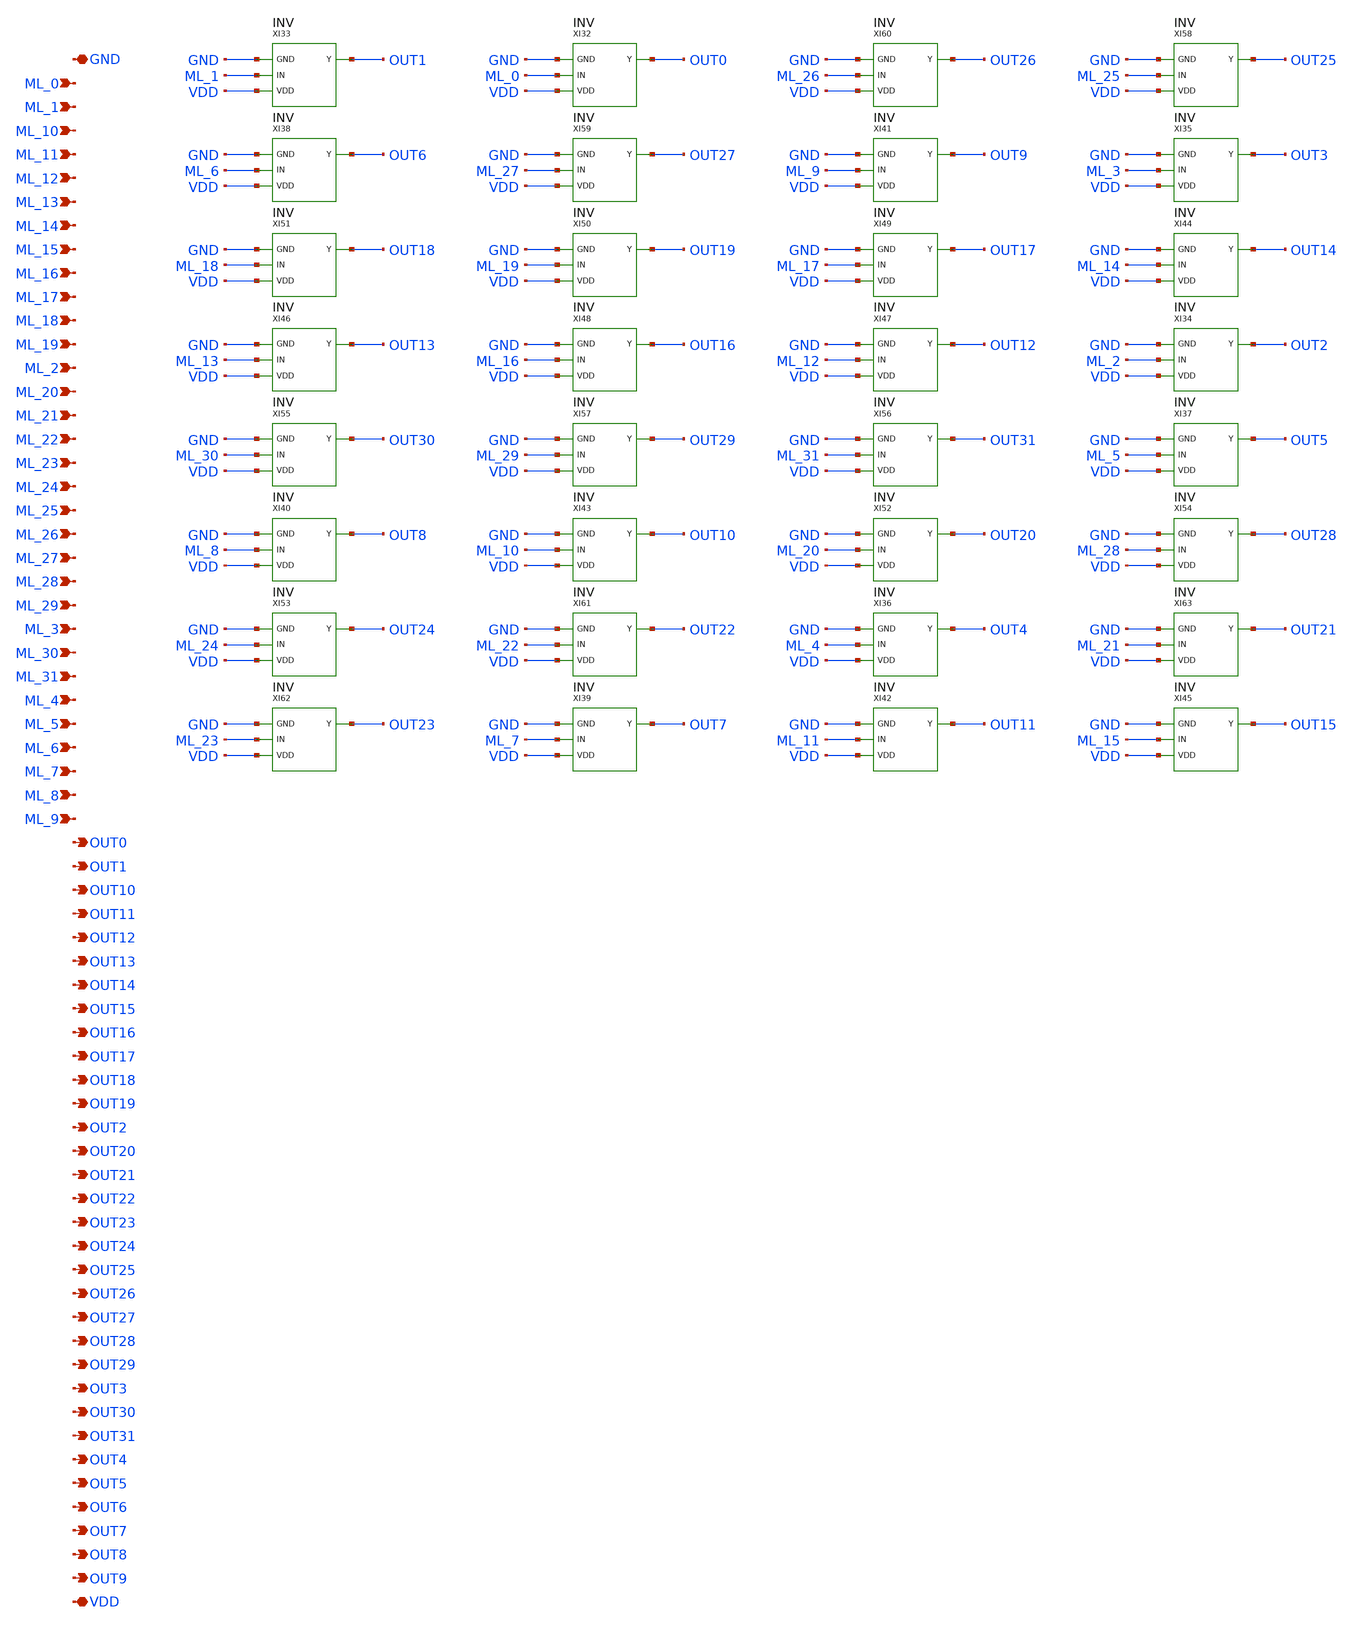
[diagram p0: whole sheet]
** sch_path: SoC6169-main/schematic/xschem/inverter_sens.sch
* Copyright 2026 USFQ CAM team
* Licensed under the Apache License, Version 2.0 (the "License");
* you may not use this file except in compliance with the License.
* You may obtain a copy of the License at
* https://www.apache.org/licenses/LICENSE-2.0
* Unless required by applicable law or agreed to in writing, software
* distributed under the License is distributed on an "AS IS" BASIS,
* WITHOUT WARRANTIES OR CONDITIONS OF ANY KIND, either express or implied.
* See the License for the specific language governing permissions and
* limitations under the License.
**.subckt inverter_sens GND ML_0 ML_1 ML_10 ML_11 ML_12 ML_13 ML_14 ML_15 ML_16 ML_17 ML_18 ML_19
*+ ML_2 ML_20 ML_21 ML_22 ML_23 ML_24 ML_25 ML_26 ML_27 ML_28 ML_29 ML_3 ML_30 ML_31 ML_4 ML_5 ML_6 ML_7
*+ ML_8 ML_9 OUT0 OUT1 OUT10 OUT11 OUT12 OUT13 OUT14 OUT15 OUT16 OUT17 OUT18 OUT19 OUT2 OUT20 OUT21 OUT22
*+ OUT23 OUT24 OUT25 OUT26 OUT27 OUT28 OUT29 OUT3 OUT30 OUT31 OUT4 OUT5 OUT6 OUT7 OUT8 OUT9 VDD
*.iopin GND
*.ipin ML_0
*.ipin ML_1
*.ipin ML_10
*.ipin ML_11
*.ipin ML_12
*.ipin ML_13
*.ipin ML_14
*.ipin ML_15
*.ipin ML_16
*.ipin ML_17
*.ipin ML_18
*.ipin ML_19
*.ipin ML_2
*.ipin ML_20
*.ipin ML_21
*.ipin ML_22
*.ipin ML_23
*.ipin ML_24
*.ipin ML_25
*.ipin ML_26
*.ipin ML_27
*.ipin ML_28
*.ipin ML_29
*.ipin ML_3
*.ipin ML_30
*.ipin ML_31
*.ipin ML_4
*.ipin ML_5
*.ipin ML_6
*.ipin ML_7
*.ipin ML_8
*.ipin ML_9
*.opin OUT0
*.opin OUT1
*.opin OUT10
*.opin OUT11
*.opin OUT12
*.opin OUT13
*.opin OUT14
*.opin OUT15
*.opin OUT16
*.opin OUT17
*.opin OUT18
*.opin OUT19
*.opin OUT2
*.opin OUT20
*.opin OUT21
*.opin OUT22
*.opin OUT23
*.opin OUT24
*.opin OUT25
*.opin OUT26
*.opin OUT27
*.opin OUT28
*.opin OUT29
*.opin OUT3
*.opin OUT30
*.opin OUT31
*.opin OUT4
*.opin OUT5
*.opin OUT6
*.opin OUT7
*.opin OUT8
*.opin OUT9
*.iopin VDD
XI33 GND ML_1 VDD OUT1 INV
XI32 GND ML_0 VDD OUT0 INV
XI60 GND ML_26 VDD OUT26 INV
XI58 GND ML_25 VDD OUT25 INV
XI38 GND ML_6 VDD OUT6 INV
XI59 GND ML_27 VDD OUT27 INV
XI41 GND ML_9 VDD OUT9 INV
XI35 GND ML_3 VDD OUT3 INV
XI51 GND ML_18 VDD OUT18 INV
XI50 GND ML_19 VDD OUT19 INV
XI49 GND ML_17 VDD OUT17 INV
XI44 GND ML_14 VDD OUT14 INV
XI46 GND ML_13 VDD OUT13 INV
XI48 GND ML_16 VDD OUT16 INV
XI47 GND ML_12 VDD OUT12 INV
XI34 GND ML_2 VDD OUT2 INV
XI55 GND ML_30 VDD OUT30 INV
XI57 GND ML_29 VDD OUT29 INV
XI56 GND ML_31 VDD OUT31 INV
XI37 GND ML_5 VDD OUT5 INV
XI40 GND ML_8 VDD OUT8 INV
XI43 GND ML_10 VDD OUT10 INV
XI52 GND ML_20 VDD OUT20 INV
XI54 GND ML_28 VDD OUT28 INV
XI53 GND ML_24 VDD OUT24 INV
XI61 GND ML_22 VDD OUT22 INV
XI36 GND ML_4 VDD OUT4 INV
XI63 GND ML_21 VDD OUT21 INV
XI62 GND ML_23 VDD OUT23 INV
XI39 GND ML_7 VDD OUT7 INV
XI42 GND ML_11 VDD OUT11 INV
XI45 GND ML_15 VDD OUT15 INV
**.ends

* expanding   symbol:  INV.sym # of pins=4
** sym_path: SoC6169-main/schematic/xschem/INV.sym
** sch_path: SoC6169-main/schematic/xschem/INV.sch
.subckt INV GND IN VDD Y
*.iopin GND
*.ipin IN
*.iopin VDD
*.opin Y
XMN0 Y IN GND GND sg13_lv_nmos w=200n l=130n ng=1 m=1 mm_ok=1
XMP0 Y IN VDD VDD sg13_lv_pmos w=400n l=130n ng=1 m=1 mm_ok=1
.ends

.end
